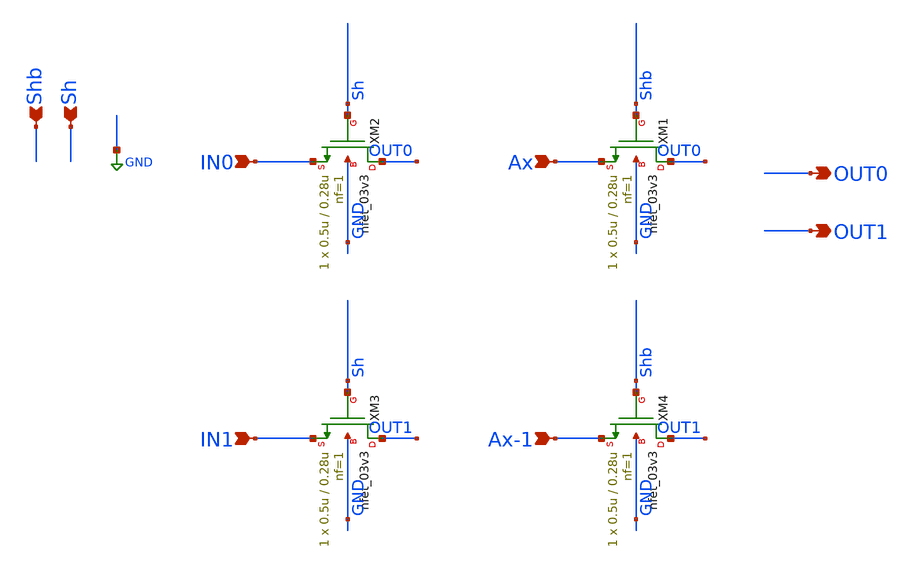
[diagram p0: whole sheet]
** sch_path: 2BIT.sch
**.subckt 2BIT Sh Shb OUT0 Ax IN0 Ax-1 IN1 OUT1
*.ipin Sh
*.ipin Shb
*.opin OUT0
*.ipin Ax
*.ipin IN0
*.ipin Ax-1
*.ipin IN1
*.opin OUT1
XM2 OUT0 Sh IN0 GND nfet_03v3 L=0.28u W=0.5u nf=1 ad='int((nf+1)/2) * W/nf * 0.18u' as='int((nf+2)/2) * W/nf * 0.18u'
+ pd='2*int((nf+1)/2) * (W/nf + 0.18u)' ps='2*int((nf+2)/2) * (W/nf + 0.18u)' nrd='0.18u / W' nrs='0.18u / W'
+ sa=0 sb=0 sd=0 m=1
XM1 OUT0 Shb Ax GND nfet_03v3 L=0.28u W=0.5u nf=1 ad='int((nf+1)/2) * W/nf * 0.18u' as='int((nf+2)/2) * W/nf * 0.18u'
+ pd='2*int((nf+1)/2) * (W/nf + 0.18u)' ps='2*int((nf+2)/2) * (W/nf + 0.18u)' nrd='0.18u / W' nrs='0.18u / W'
+ sa=0 sb=0 sd=0 m=1
XM3 OUT1 Sh IN1 GND nfet_03v3 L=0.28u W=0.5u nf=1 ad='int((nf+1)/2) * W/nf * 0.18u' as='int((nf+2)/2) * W/nf * 0.18u'
+ pd='2*int((nf+1)/2) * (W/nf + 0.18u)' ps='2*int((nf+2)/2) * (W/nf + 0.18u)' nrd='0.18u / W' nrs='0.18u / W'
+ sa=0 sb=0 sd=0 m=1
XM4 OUT1 Shb Ax-1 GND nfet_03v3 L=0.28u W=0.5u nf=1 ad='int((nf+1)/2) * W/nf * 0.18u' as='int((nf+2)/2) * W/nf * 0.18u'
+ pd='2*int((nf+1)/2) * (W/nf + 0.18u)' ps='2*int((nf+2)/2) * (W/nf + 0.18u)' nrd='0.18u / W' nrs='0.18u / W'
+ sa=0 sb=0 sd=0 m=1
**.ends
.GLOBAL GND
.end
